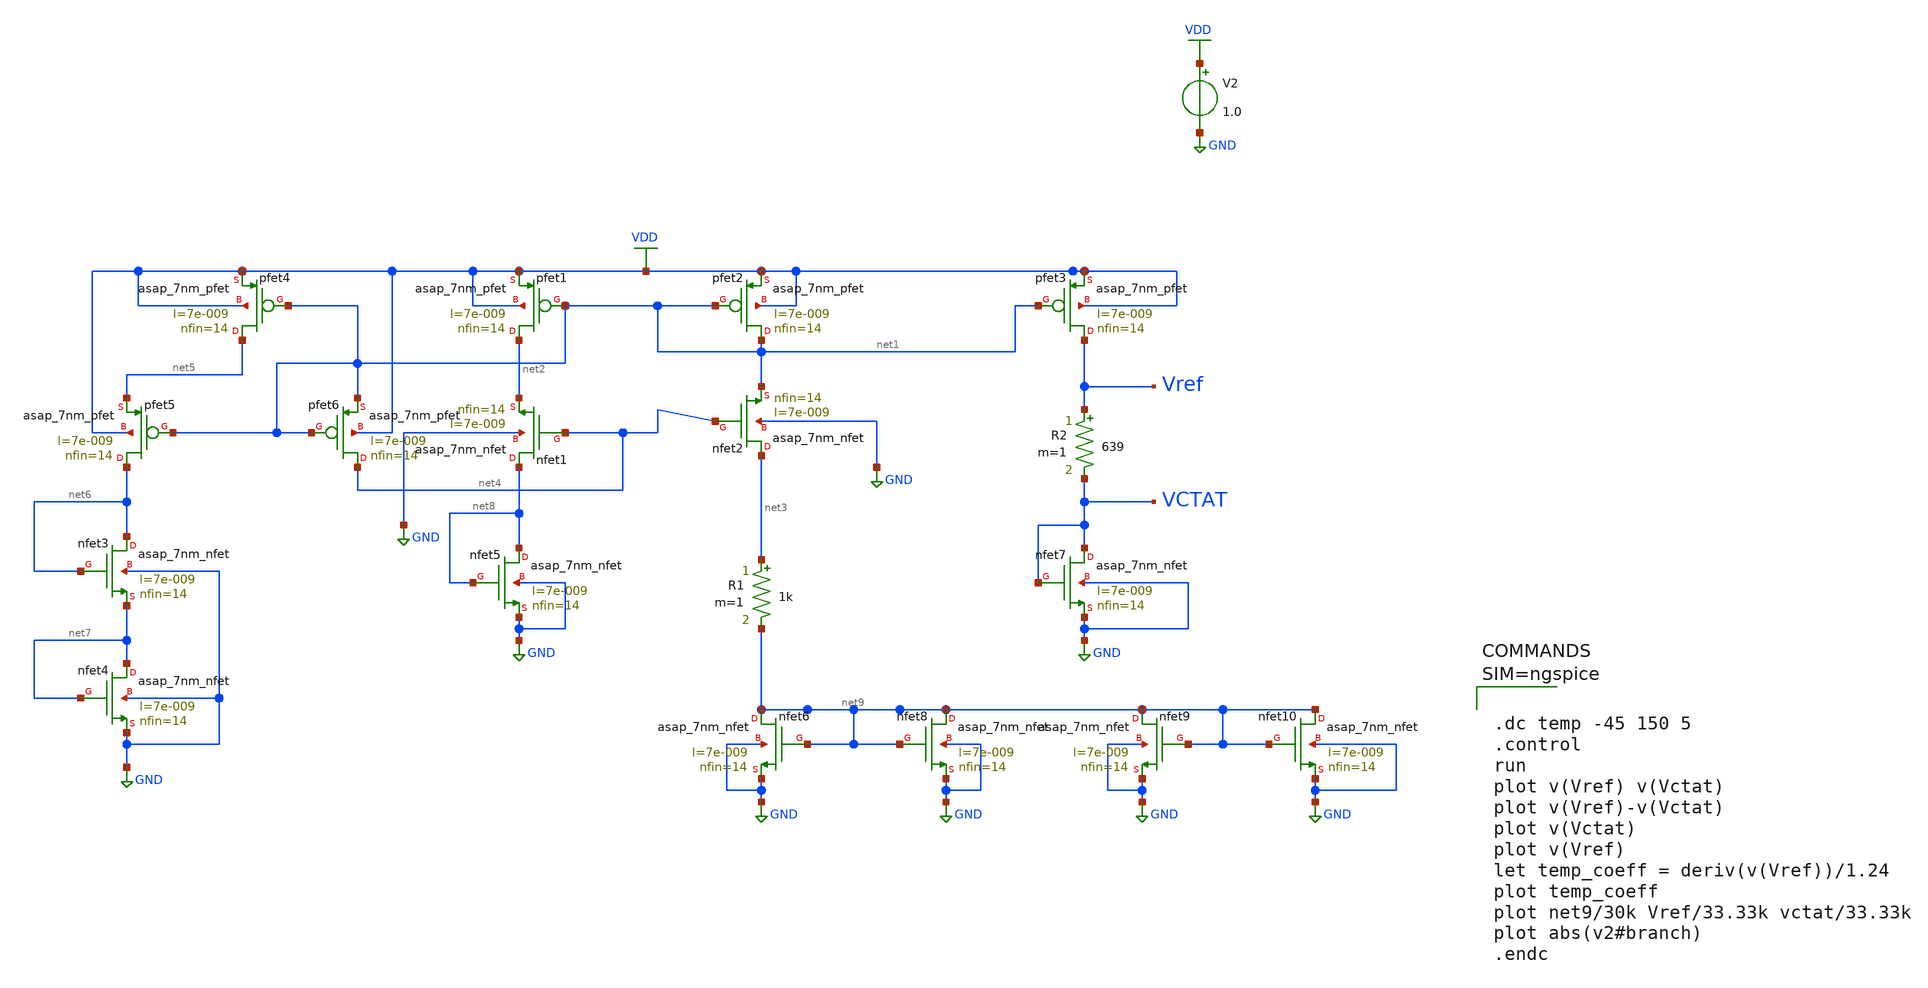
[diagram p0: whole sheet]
** sch_path: module3/bandgap_ref.sch
**.subckt bandgap_ref
Xpfet1 net2 net1 VDD VDD asap_7nm_pfet l=7e-009 nfin=14
Xpfet2 net1 net1 VDD VDD asap_7nm_pfet l=7e-009 nfin=14
Xpfet3 Vref net1 VDD VDD asap_7nm_pfet l=7e-009 nfin=14
Xpfet4 net5 net1 VDD VDD asap_7nm_pfet l=7e-009 nfin=14
Xpfet5 net6 net1 net5 VDD asap_7nm_pfet l=7e-009 nfin=14
Xpfet6 net4 net1 net1 VDD asap_7nm_pfet l=7e-009 nfin=14
Xnfet1 net8 net4 net2 GND asap_7nm_nfet l=7e-009 nfin=14
Xnfet2 net3 net4 net1 GND asap_7nm_nfet l=7e-009 nfin=14
Xnfet3 net6 net6 net7 GND asap_7nm_nfet l=7e-009 nfin=14
Xnfet4 net7 net7 GND GND asap_7nm_nfet l=7e-009 nfin=14
Xnfet5 net8 net8 GND GND asap_7nm_nfet l=7e-009 nfin=14
R1 net3 net9 1k m=1
Xnfet6 net9 net9 GND GND asap_7nm_nfet l=7e-009 nfin=14
R2 Vref VCTAT 639 m=1
Xnfet7 VCTAT VCTAT GND GND asap_7nm_nfet l=7e-009 nfin=14
Xnfet8 net9 net9 GND GND asap_7nm_nfet l=7e-009 nfin=14
Xnfet9 net9 net9 GND GND asap_7nm_nfet l=7e-009 nfin=14
Xnfet10 net9 net9 GND GND asap_7nm_nfet l=7e-009 nfin=14
V2 VDD GND 1.0
**** begin user architecture code



.dc temp -45 150 5
.control
run
plot v(Vref) v(Vctat)
plot v(Vref)-v(Vctat)
plot v(Vctat)
plot v(Vref)
let temp_coeff = deriv(v(Vref))/1.24
plot temp_coeff
plot net9/30k Vref/33.33k vctat/33.33k
plot abs(v2#branch)
.endc



**** end user architecture code
**.ends
.GLOBAL VDD
.GLOBAL GND
.end
